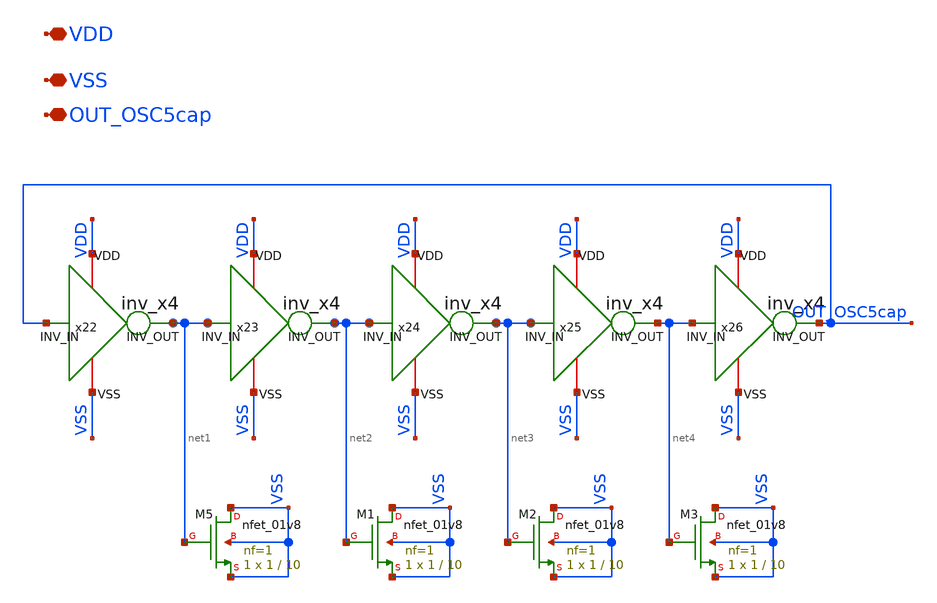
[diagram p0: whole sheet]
** sch_path: xschem/OSC5cap.sch
**.subckt OSC5cap VDD VSS OUT_OSC5cap
*.iopin VDD
*.iopin VSS
*.iopin OUT_OSC5cap
x22 VDD VSS net1 OUT_OSC5cap inv_x4
x23 VDD VSS net2 net1 inv_x4
x24 VDD VSS net3 net2 inv_x4
x25 VDD VSS net4 net3 inv_x4
x26 VDD VSS OUT_OSC5cap net4 inv_x4
XM5 VSS net1 VSS VSS sky130_fd_pr__nfet_01v8 L=10 W=1 nf=1 ad='int((nf+1)/2) * W/nf * 0.29' as='int((nf+2)/2) * W/nf * 0.29'
+ pd='2*int((nf+1)/2) * (W/nf + 0.29)' ps='2*int((nf+2)/2) * (W/nf + 0.29)' nrd='0.29 / W' nrs='0.29 / W'
+ sa=0 sb=0 sd=0 mult=1 m=1
XM1 VSS net2 VSS VSS sky130_fd_pr__nfet_01v8 L=10 W=1 nf=1 ad='int((nf+1)/2) * W/nf * 0.29' as='int((nf+2)/2) * W/nf * 0.29'
+ pd='2*int((nf+1)/2) * (W/nf + 0.29)' ps='2*int((nf+2)/2) * (W/nf + 0.29)' nrd='0.29 / W' nrs='0.29 / W'
+ sa=0 sb=0 sd=0 mult=1 m=1
XM2 VSS net3 VSS VSS sky130_fd_pr__nfet_01v8 L=10 W=1 nf=1 ad='int((nf+1)/2) * W/nf * 0.29' as='int((nf+2)/2) * W/nf * 0.29'
+ pd='2*int((nf+1)/2) * (W/nf + 0.29)' ps='2*int((nf+2)/2) * (W/nf + 0.29)' nrd='0.29 / W' nrs='0.29 / W'
+ sa=0 sb=0 sd=0 mult=1 m=1
XM3 VSS net4 VSS VSS sky130_fd_pr__nfet_01v8 L=10 W=1 nf=1 ad='int((nf+1)/2) * W/nf * 0.29' as='int((nf+2)/2) * W/nf * 0.29'
+ pd='2*int((nf+1)/2) * (W/nf + 0.29)' ps='2*int((nf+2)/2) * (W/nf + 0.29)' nrd='0.29 / W' nrs='0.29 / W'
+ sa=0 sb=0 sd=0 mult=1 m=1
**.ends

* expanding   symbol:  inv_x4.sym # of pins=4
** sym_path: xschem/inv_x4.sym
** sch_path: xschem/inv_x4.sch
.subckt inv_x4 VDD VSS INV_OUT INV_IN
*.ipin INV_IN
*.opin INV_OUT
*.iopin VDD
*.iopin VSS
XM3 INV_OUT INV_IN VDD VDD sky130_fd_pr__pfet_01v8 L=10 W=2 nf=1 ad='int((nf+1)/2) * W/nf * 0.29' as='int((nf+2)/2) * W/nf * 0.29'
+ pd='2*int((nf+1)/2) * (W/nf + 0.29)' ps='2*int((nf+2)/2) * (W/nf + 0.29)' nrd='0.29 / W' nrs='0.29 / W'
+ sa=0 sb=0 sd=0 mult=1 m=1
XM5 INV_OUT INV_IN VSS VSS sky130_fd_pr__nfet_01v8 L=10 W=1 nf=1 ad='int((nf+1)/2) * W/nf * 0.29' as='int((nf+2)/2) * W/nf * 0.29'
+ pd='2*int((nf+1)/2) * (W/nf + 0.29)' ps='2*int((nf+2)/2) * (W/nf + 0.29)' nrd='0.29 / W' nrs='0.29 / W'
+ sa=0 sb=0 sd=0 mult=1 m=1
.ends

.end
